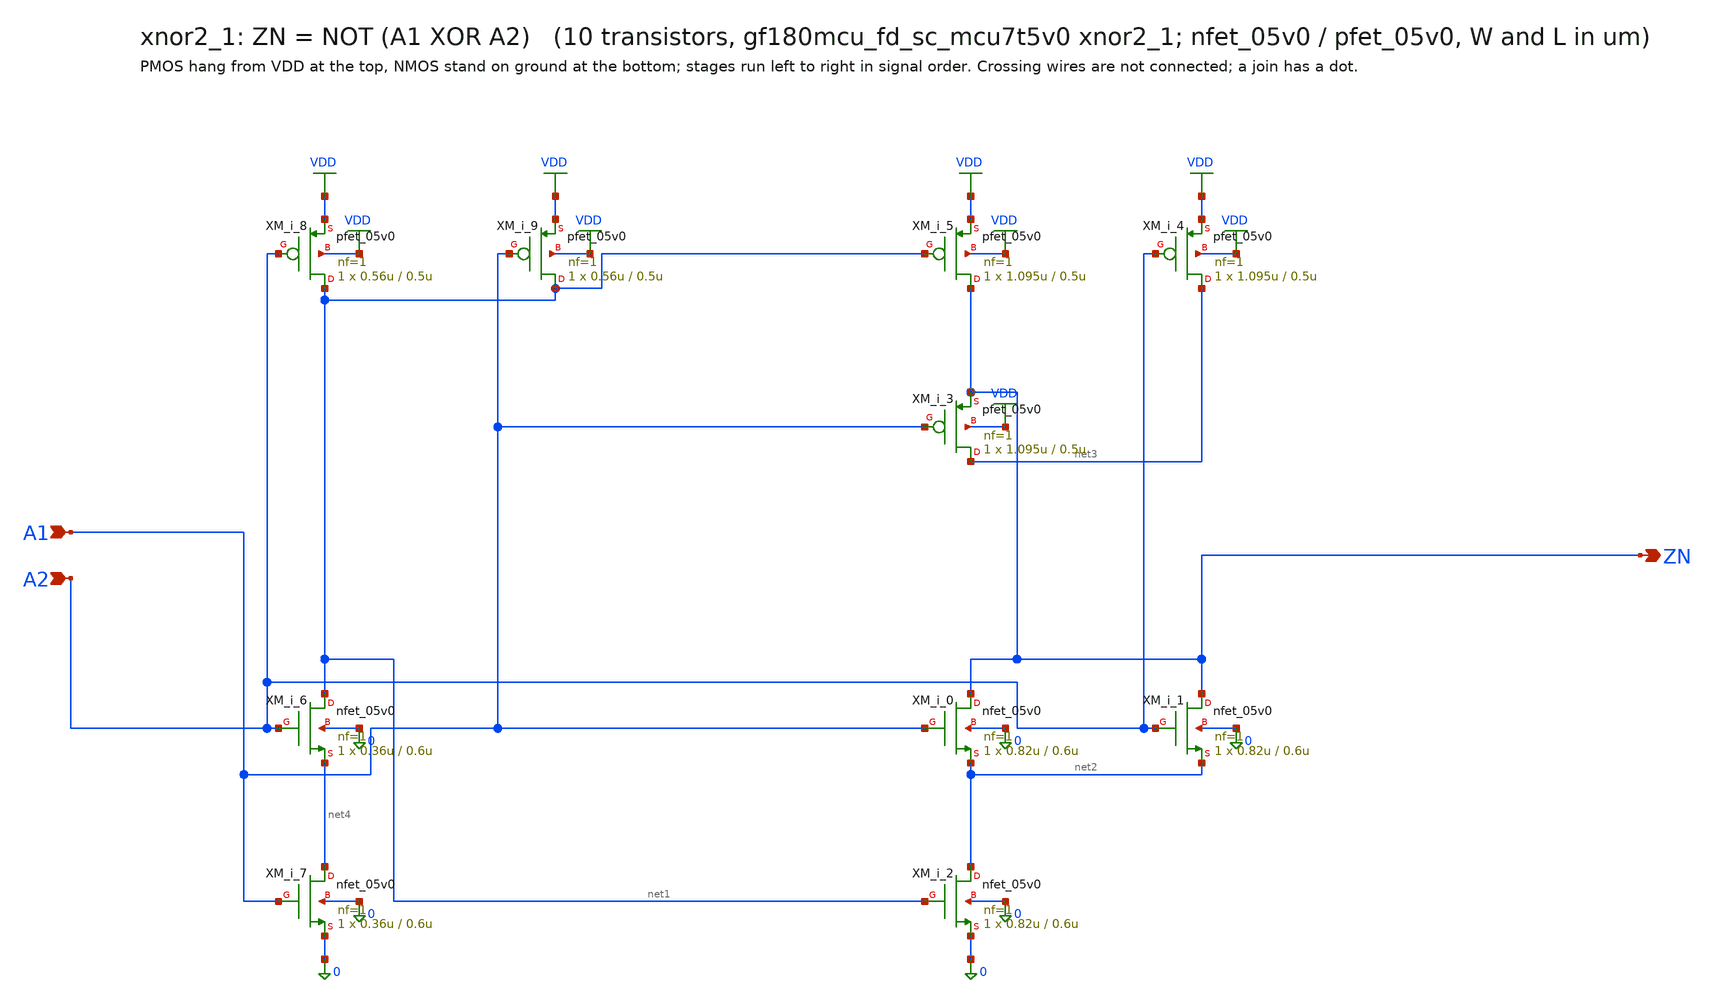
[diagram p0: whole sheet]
** sch_path: xschem/cells_tx/xnor2_1.sch
**.subckt xnor2_1 A1 A2 ZN
*.ipin A1
*.ipin A2
*.opin ZN
XM_i_6 net1 A2 net4 0 nfet_05v0 L=0.6u W=0.36u nf=1 ad=1.8e-13 as=1.8e-13 pd=1.72e-06 ps=1.72e-06
+ nrd=0 nrs=0 sa=0 sb=0 sd=0 m=1
XM_i_7 net4 A1 0 0 nfet_05v0 L=0.6u W=0.36u nf=1 ad=1.8e-13 as=1.8e-13 pd=1.72e-06 ps=1.72e-06 nrd=0
+ nrs=0 sa=0 sb=0 sd=0 m=1
XM_i_2 net2 net1 0 0 nfet_05v0 L=0.6u W=0.82u nf=1 ad=4.1e-13 as=4.1e-13 pd=2.64e-06 ps=2.64e-06
+ nrd=0 nrs=0 sa=0 sb=0 sd=0 m=1
XM_i_0 ZN A1 net2 0 nfet_05v0 L=0.6u W=0.82u nf=1 ad=4.1e-13 as=4.1e-13 pd=2.64e-06 ps=2.64e-06
+ nrd=0 nrs=0 sa=0 sb=0 sd=0 m=1
XM_i_1 ZN A2 net2 0 nfet_05v0 L=0.6u W=0.82u nf=1 ad=4.1e-13 as=4.1e-13 pd=2.64e-06 ps=2.64e-06
+ nrd=0 nrs=0 sa=0 sb=0 sd=0 m=1
XM_i_8 net1 A2 VDD VDD pfet_05v0 L=0.5u W=0.56u nf=1 ad=2.8e-13 as=2.8e-13 pd=2.12e-06 ps=2.12e-06
+ nrd=0 nrs=0 sa=0 sb=0 sd=0 m=1
XM_i_9 net1 A1 VDD VDD pfet_05v0 L=0.5u W=0.56u nf=1 ad=2.8e-13 as=2.8e-13 pd=2.12e-06 ps=2.12e-06
+ nrd=0 nrs=0 sa=0 sb=0 sd=0 m=1
XM_i_5 ZN net1 VDD VDD pfet_05v0 L=0.5u W=1.095u nf=1 ad=5.475e-13 as=5.475e-13 pd=3.19e-06
+ ps=3.19e-06 nrd=0 nrs=0 sa=0 sb=0 sd=0 m=1
XM_i_3 net3 A1 ZN VDD pfet_05v0 L=0.5u W=1.095u nf=1 ad=5.475e-13 as=5.475e-13 pd=3.19e-06
+ ps=3.19e-06 nrd=0 nrs=0 sa=0 sb=0 sd=0 m=1
XM_i_4 net3 A2 VDD VDD pfet_05v0 L=0.5u W=1.095u nf=1 ad=5.475e-13 as=5.475e-13 pd=3.19e-06
+ ps=3.19e-06 nrd=0 nrs=0 sa=0 sb=0 sd=0 m=1
**.ends
.GLOBAL VDD
.end
